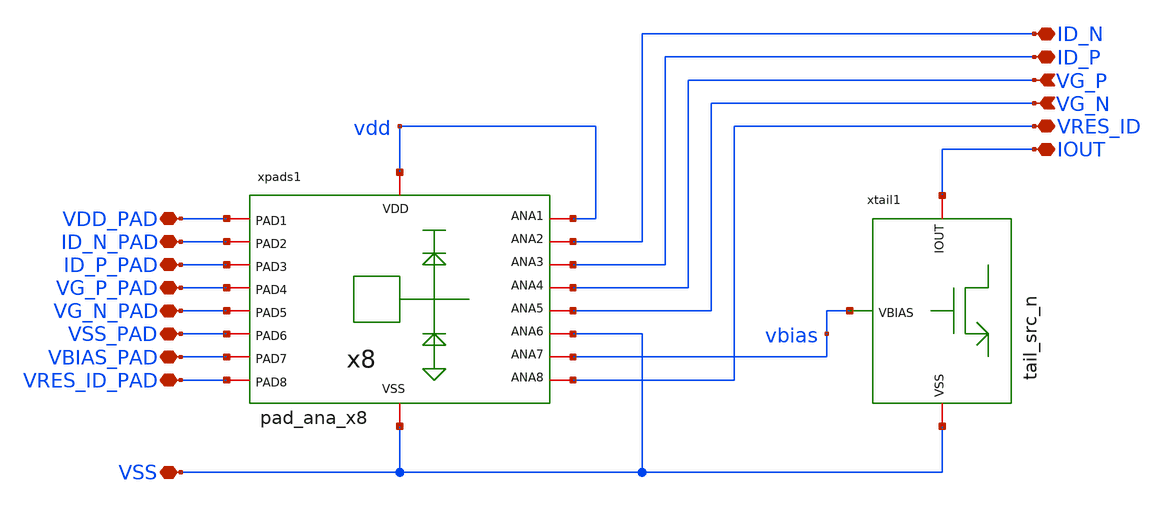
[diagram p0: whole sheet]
** sch_path: JKU_TC1/design_data/sfl-test-cells/xschem/testcells/tb_nmos.sch
**.subckt tb_nmos VDD_PAD ID_N_PAD ID_P_PAD VG_P_PAD VG_N_PAD VSS_PAD VBIAS_PAD VRES_ID_PAD VSS IOUT
*+ VRES_ID ID_N ID_P VG_P VG_N
*.iopin VDD_PAD
*.iopin ID_N_PAD
*.iopin ID_P_PAD
*.iopin VG_P_PAD
*.iopin VG_N_PAD
*.iopin VSS_PAD
*.iopin VBIAS_PAD
*.iopin VRES_ID_PAD
*.iopin VSS
*.iopin IOUT
*.iopin VRES_ID
*.iopin ID_N
*.iopin ID_P
*.ipin VG_P
*.ipin VG_N
xpads1 VSS_PAD VDD_PAD VG_P_PAD VG_N_PAD ID_N_PAD ID_P_PAD VBIAS_PAD VRES_ID_PAD vdd VSS VG_N VG_P
+ VRES_ID ID_P vbias VSS ID_N vdd pad_ana_x8
xtail1 IOUT vbias VSS tail_src_n
**.ends

* expanding   symbol:  pads/pad_ana_x8.sym # of pins=18
** sym_path: JKU_TC1/design_data/xschem/pads/pad_ana_x8.sym
** sch_path: JKU_TC1/design_data/xschem/pads/pad_ana_x8.sch
.subckt pad_ana_x8 PAD6 PAD1 PAD4 PAD5 PAD2 PAD3 PAD7 PAD8 VDD VSS ANA5 ANA4 ANA8 ANA3 ANA7 ANA6
+ ANA2 ANA1
*.iopin VDD
*.iopin VSS
*.iopin ANA1
*.iopin ANA2
*.iopin ANA3
*.iopin ANA4
*.iopin ANA5
*.iopin ANA6
*.iopin ANA7
*.iopin ANA8
*.iopin PAD1
*.iopin PAD2
*.iopin PAD3
*.iopin PAD4
*.iopin PAD5
*.iopin PAD6
*.iopin PAD7
*.iopin PAD8
xpad1 VDD PAD1 ANA1 VSS pad_ana
xpad2 VDD PAD2 ANA2 VSS pad_ana
xpad3 VDD PAD3 ANA3 VSS pad_ana
xpad4 VDD PAD4 ANA4 VSS pad_ana
xpad5 VDD PAD5 ANA5 VSS pad_ana
xpad6 VDD PAD6 ANA6 VSS pad_ana
xpad7 VDD PAD7 ANA7 VSS pad_ana
xpad8 VDD PAD8 ANA8 VSS pad_ana
.ends


* expanding   symbol:  tailsrcs/tail_src_n.sym # of pins=3
** sym_path: JKU_TC1/design_data/sfl-test-cells/xschem/tailsrcs/tail_src_n.sym
** sch_path: JKU_TC1/design_data/sfl-test-cells/xschem/tailsrcs/tail_src_n.sch
.subckt tail_src_n IOUT VBIAS VSS
*.ipin VBIAS
*.iopin VSS
*.iopin IOUT
XM1 VSS VBIAS IOUT VSS sg13_lv_nmos w=160u l=10u ng=20 m=5 mm_ok=1
XM2 VSS VBIAS VSS VSS sg13_lv_nmos w=8u l=10u ng=1 m=10 mm_ok=1
XM3 VSS VBIAS VSS VSS sg13_lv_nmos w=176u l=10u ng=22 m=2 mm_ok=1
.ends


* expanding   symbol:  pads/pad_ana.sym # of pins=4
** sym_path: JKU_TC1/design_data/xschem/pads/pad_ana.sym
** sch_path: JKU_TC1/design_data/xschem/pads/pad_ana.sch
.subckt pad_ana VDD PAD ANA VSS
*.iopin VSS
*.iopin PAD
*.iopin VDD
*.iopin ANA
XC1 VDD PAD cparasitic C=20f
XC2 PAD VSS cparasitic C=20f
R1 PAD ANA 1e-6 m=1
R2 PAD ANA 1e-6 m=1
xesd1 VDD PAD VSS pad_diodes
.ends


* expanding   symbol:  pads/pad_diodes.sym # of pins=3
** sym_path: JKU_TC1/design_data/xschem/pads/pad_diodes.sym
** sch_path: JKU_TC1/design_data/xschem/pads/pad_diodes.sch
.subckt pad_diodes VDD PAD VSS
*.iopin VDD
*.iopin VSS
*.iopin PAD
XXD1 PAD VDD dantenna l=780n w=780n
XXD2 VSS PAD dantenna l=780n w=780n
.ends

.end
